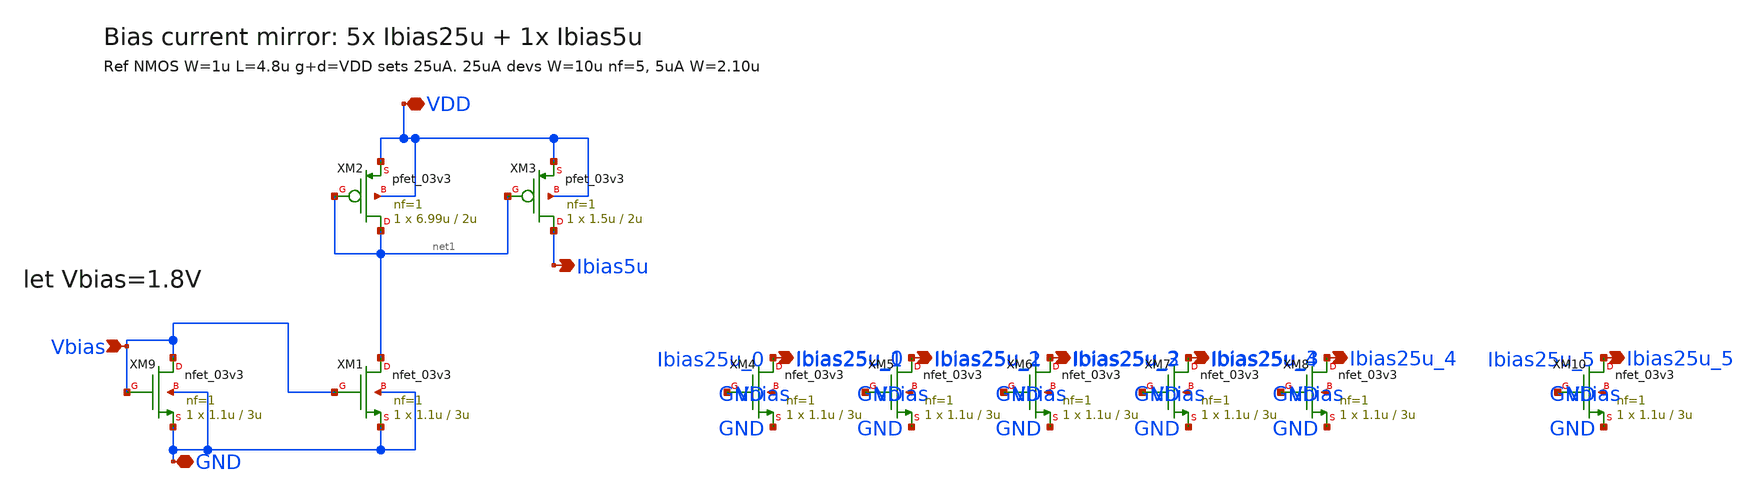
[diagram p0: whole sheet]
** sch_path: ps-bias/jz_bias.sch
**.subckt jz_bias Ibias25u_0 Ibias25u_1 Ibias25u_2 Ibias25u_3 Ibias25u_4 Ibias5u VDD GND Vbias
*+ Ibias25u_5
*.opin Ibias25u_0
*.opin Ibias25u_1
*.opin Ibias25u_2
*.opin Ibias25u_3
*.opin Ibias25u_4
*.opin Ibias5u
*.iopin VDD
*.iopin GND
*.ipin Vbias
*.opin Ibias25u_5
XM2 net1 net1 VDD VDD pfet_03v3 L=2u W=6.99u nf=1 ad='int((nf+1)/2) * W/nf * 0.18u' as='int((nf+2)/2) * W/nf * 0.18u'
+ pd='2*int((nf+1)/2) * (W/nf + 0.18u)' ps='2*int((nf+2)/2) * (W/nf + 0.18u)' nrd='0.18u / W' nrs='0.18u / W'
+ sa=0 sb=0 sd=0 m=1
XM3 Ibias5u net1 VDD VDD pfet_03v3 L=2u W=1.5u nf=1 ad='int((nf+1)/2) * W/nf * 0.18u' as='int((nf+2)/2) * W/nf * 0.18u'
+ pd='2*int((nf+1)/2) * (W/nf + 0.18u)' ps='2*int((nf+2)/2) * (W/nf + 0.18u)' nrd='0.18u / W' nrs='0.18u / W'
+ sa=0 sb=0 sd=0 m=1
XM9 Vbias Vbias GND GND nfet_03v3 L=3u W=1.1u nf=1 ad='int((nf+1)/2) * W/nf * 0.18u' as='int((nf+2)/2) * W/nf * 0.18u'
+ pd='2*int((nf+1)/2) * (W/nf + 0.18u)' ps='2*int((nf+2)/2) * (W/nf + 0.18u)' nrd='0.18u / W' nrs='0.18u / W'
+ sa=0 sb=0 sd=0 m=1
XM1 net1 Vbias GND GND nfet_03v3 L=3u W=1.1u nf=1 ad='int((nf+1)/2) * W/nf * 0.18u' as='int((nf+2)/2) * W/nf * 0.18u'
+ pd='2*int((nf+1)/2) * (W/nf + 0.18u)' ps='2*int((nf+2)/2) * (W/nf + 0.18u)' nrd='0.18u / W' nrs='0.18u / W'
+ sa=0 sb=0 sd=0 m=1
XM4 Ibias25u_0 Vbias GND GND nfet_03v3 L=3u W=1.1u nf=1 ad='int((nf+1)/2) * W/nf * 0.18u' as='int((nf+2)/2) * W/nf * 0.18u'
+ pd='2*int((nf+1)/2) * (W/nf + 0.18u)' ps='2*int((nf+2)/2) * (W/nf + 0.18u)' nrd='0.18u / W' nrs='0.18u / W'
+ sa=0 sb=0 sd=0 m=1
XM5 Ibias25u_1 Vbias GND GND nfet_03v3 L=3u W=1.1u nf=1 ad='int((nf+1)/2) * W/nf * 0.18u' as='int((nf+2)/2) * W/nf * 0.18u'
+ pd='2*int((nf+1)/2) * (W/nf + 0.18u)' ps='2*int((nf+2)/2) * (W/nf + 0.18u)' nrd='0.18u / W' nrs='0.18u / W'
+ sa=0 sb=0 sd=0 m=1
XM6 Ibias25u_2 Vbias GND GND nfet_03v3 L=3u W=1.1u nf=1 ad='int((nf+1)/2) * W/nf * 0.18u' as='int((nf+2)/2) * W/nf * 0.18u'
+ pd='2*int((nf+1)/2) * (W/nf + 0.18u)' ps='2*int((nf+2)/2) * (W/nf + 0.18u)' nrd='0.18u / W' nrs='0.18u / W'
+ sa=0 sb=0 sd=0 m=1
XM7 Ibias25u_3 Vbias GND GND nfet_03v3 L=3u W=1.1u nf=1 ad='int((nf+1)/2) * W/nf * 0.18u' as='int((nf+2)/2) * W/nf * 0.18u'
+ pd='2*int((nf+1)/2) * (W/nf + 0.18u)' ps='2*int((nf+2)/2) * (W/nf + 0.18u)' nrd='0.18u / W' nrs='0.18u / W'
+ sa=0 sb=0 sd=0 m=1
XM8 Ibias25u_4 Vbias GND GND nfet_03v3 L=3u W=1.1u nf=1 ad='int((nf+1)/2) * W/nf * 0.18u' as='int((nf+2)/2) * W/nf * 0.18u'
+ pd='2*int((nf+1)/2) * (W/nf + 0.18u)' ps='2*int((nf+2)/2) * (W/nf + 0.18u)' nrd='0.18u / W' nrs='0.18u / W'
+ sa=0 sb=0 sd=0 m=1
XM10 Ibias25u_5 Vbias GND GND nfet_03v3 L=3u W=1.1u nf=1 ad='int((nf+1)/2) * W/nf * 0.18u' as='int((nf+2)/2) * W/nf * 0.18u'
+ pd='2*int((nf+1)/2) * (W/nf + 0.18u)' ps='2*int((nf+2)/2) * (W/nf + 0.18u)' nrd='0.18u / W' nrs='0.18u / W'
+ sa=0 sb=0 sd=0 m=1
**.ends
.end
